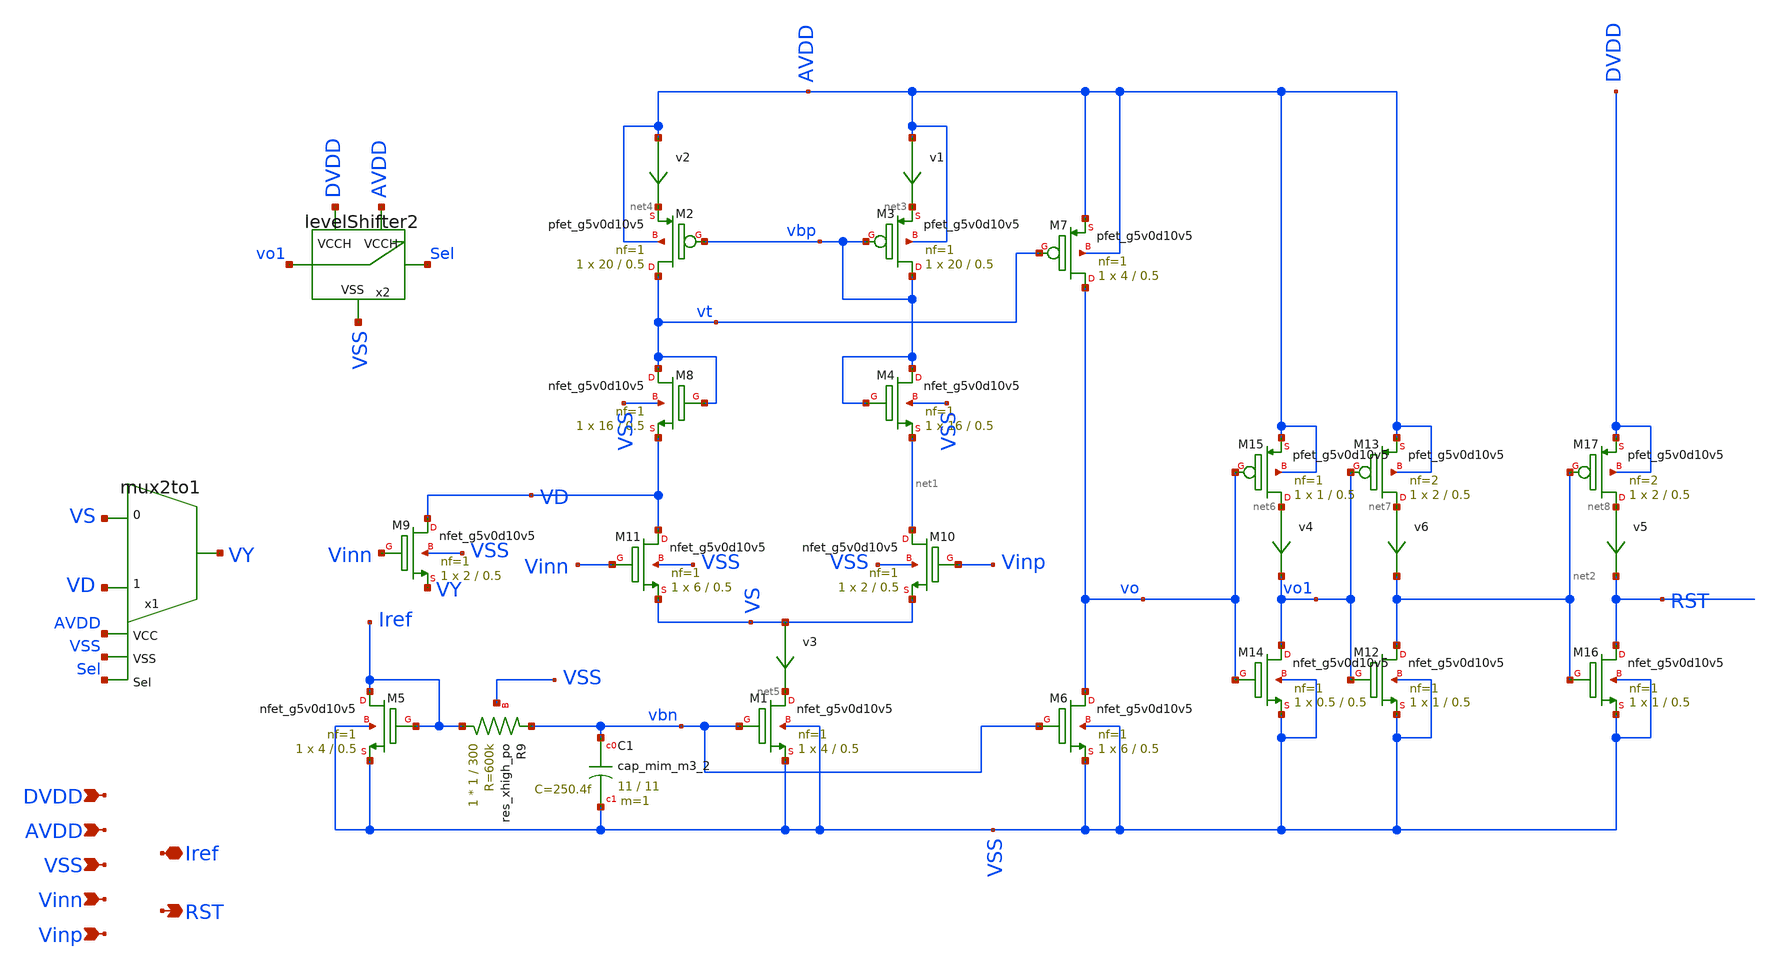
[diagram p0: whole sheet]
** sch_path: xschem/comparator_swu1.sch
**.subckt comparator_swu1 AVDD RST VSS Iref Vinn Vinp DVDD
*.ipin AVDD
*.opin RST
*.ipin VSS
*.iopin Iref
*.ipin Vinn
*.ipin Vinp
*.ipin DVDD
v1 AVDD net3 0
.save i(v1)
v2 AVDD net4 0
.save i(v2)
XM1 net5 vbn VSS VSS sky130_fd_pr__nfet_g5v0d10v5 L=0.5 W=4 nf=1 ad='int((nf+1)/2) * W/nf * 0.29' as='int((nf+2)/2) * W/nf * 0.29'
+ pd='2*int((nf+1)/2) * (W/nf + 0.29)' ps='2*int((nf+2)/2) * (W/nf + 0.29)' nrd='0.29 / W' nrs='0.29 / W'
+ sa=0 sb=0 sd=0 mult=1 m=1
XM3 vbp vbp net3 AVDD sky130_fd_pr__pfet_g5v0d10v5 L=0.5 W=20 nf=1 ad='int((nf+1)/2) * W/nf * 0.29' as='int((nf+2)/2) * W/nf * 0.29'
+ pd='2*int((nf+1)/2) * (W/nf + 0.29)' ps='2*int((nf+2)/2) * (W/nf + 0.29)' nrd='0.29 / W' nrs='0.29 / W'
+ sa=0 sb=0 sd=0 mult=1 m=1
XM2 vt vbp net4 AVDD sky130_fd_pr__pfet_g5v0d10v5 L=0.5 W=20 nf=1 ad='int((nf+1)/2) * W/nf * 0.29' as='int((nf+2)/2) * W/nf * 0.29'
+ pd='2*int((nf+1)/2) * (W/nf + 0.29)' ps='2*int((nf+2)/2) * (W/nf + 0.29)' nrd='0.29 / W' nrs='0.29 / W'
+ sa=0 sb=0 sd=0 mult=1 m=1
v4 net6 vo1 0
.save i(v4)
XM9 VD Vinn VY VSS sky130_fd_pr__nfet_g5v0d10v5 L=0.5 W=2 nf=1 ad='int((nf+1)/2) * W/nf * 0.29' as='int((nf+2)/2) * W/nf * 0.29'
+ pd='2*int((nf+1)/2) * (W/nf + 0.29)' ps='2*int((nf+2)/2) * (W/nf + 0.29)' nrd='0.29 / W' nrs='0.29 / W'
+ sa=0 sb=0 sd=0 mult=1 m=1
XM10 net1 Vinp VS VSS sky130_fd_pr__nfet_g5v0d10v5 L=0.5 W=2 nf=1 ad='int((nf+1)/2) * W/nf * 0.29' as='int((nf+2)/2) * W/nf * 0.29'
+ pd='2*int((nf+1)/2) * (W/nf + 0.29)' ps='2*int((nf+2)/2) * (W/nf + 0.29)' nrd='0.29 / W' nrs='0.29 / W'
+ sa=0 sb=0 sd=0 mult=1 m=1
XM5 Iref Iref VSS VSS sky130_fd_pr__nfet_g5v0d10v5 L=0.5 W=4 nf=1 ad='int((nf+1)/2) * W/nf * 0.29' as='int((nf+2)/2) * W/nf * 0.29'
+ pd='2*int((nf+1)/2) * (W/nf + 0.29)' ps='2*int((nf+2)/2) * (W/nf + 0.29)' nrd='0.29 / W' nrs='0.29 / W'
+ sa=0 sb=0 sd=0 mult=1 m=1
XM7 vo vt AVDD AVDD sky130_fd_pr__pfet_g5v0d10v5 L=0.5 W=4 nf=1 ad='int((nf+1)/2) * W/nf * 0.29' as='int((nf+2)/2) * W/nf * 0.29'
+ pd='2*int((nf+1)/2) * (W/nf + 0.29)' ps='2*int((nf+2)/2) * (W/nf + 0.29)' nrd='0.29 / W' nrs='0.29 / W'
+ sa=0 sb=0 sd=0 mult=1 m=1
v3 VS net5 0
.save i(v3)
XM11 VD Vinn VS VSS sky130_fd_pr__nfet_g5v0d10v5 L=0.5 W=6 nf=1 ad='int((nf+1)/2) * W/nf * 0.29' as='int((nf+2)/2) * W/nf * 0.29'
+ pd='2*int((nf+1)/2) * (W/nf + 0.29)' ps='2*int((nf+2)/2) * (W/nf + 0.29)' nrd='0.29 / W' nrs='0.29 / W'
+ sa=0 sb=0 sd=0 mult=1 m=1
x1 VD VS VY AVDD VSS Sel mux2to1
XM6 vo vbn VSS VSS sky130_fd_pr__nfet_g5v0d10v5 L=0.5 W=6 nf=1 ad='int((nf+1)/2) * W/nf * 0.29' as='int((nf+2)/2) * W/nf * 0.29'
+ pd='2*int((nf+1)/2) * (W/nf + 0.29)' ps='2*int((nf+2)/2) * (W/nf + 0.29)' nrd='0.29 / W' nrs='0.29 / W'
+ sa=0 sb=0 sd=0 mult=1 m=1
v6 net7 net2 0
.save i(v6)
XM14 vo1 vo VSS VSS sky130_fd_pr__nfet_g5v0d10v5 L=0.5 W=0.5 nf=1 ad='int((nf+1)/2) * W/nf * 0.29' as='int((nf+2)/2) * W/nf * 0.29'
+ pd='2*int((nf+1)/2) * (W/nf + 0.29)' ps='2*int((nf+2)/2) * (W/nf + 0.29)' nrd='0.29 / W' nrs='0.29 / W'
+ sa=0 sb=0 sd=0 mult=1 m=1
XM15 net6 vo AVDD AVDD sky130_fd_pr__pfet_g5v0d10v5 L=0.5 W=1 nf=1 ad='int((nf+1)/2) * W/nf * 0.29' as='int((nf+2)/2) * W/nf * 0.29'
+ pd='2*int((nf+1)/2) * (W/nf + 0.29)' ps='2*int((nf+2)/2) * (W/nf + 0.29)' nrd='0.29 / W' nrs='0.29 / W'
+ sa=0 sb=0 sd=0 mult=1 m=1
XM12 net2 vo1 VSS VSS sky130_fd_pr__nfet_g5v0d10v5 L=0.5 W=1 nf=1 ad='int((nf+1)/2) * W/nf * 0.29' as='int((nf+2)/2) * W/nf * 0.29'
+ pd='2*int((nf+1)/2) * (W/nf + 0.29)' ps='2*int((nf+2)/2) * (W/nf + 0.29)' nrd='0.29 / W' nrs='0.29 / W'
+ sa=0 sb=0 sd=0 mult=1 m=1
XM13 net7 vo1 AVDD AVDD sky130_fd_pr__pfet_g5v0d10v5 L=0.5 W=2 nf=2 ad='int((nf+1)/2) * W/nf * 0.29'
+ as='int((nf+2)/2) * W/nf * 0.29' pd='2*int((nf+1)/2) * (W/nf + 0.29)' ps='2*int((nf+2)/2) * (W/nf + 0.29)'
+ nrd='0.29 / W' nrs='0.29 / W' sa=0 sb=0 sd=0 mult=1 m=1
x2 vo1 Sel DVDD VSS AVDD levelShifter2
v5 net8 RST 0
.save i(v5)
XM16 RST net2 VSS VSS sky130_fd_pr__nfet_g5v0d10v5 L=0.5 W=1 nf=1 ad='int((nf+1)/2) * W/nf * 0.29' as='int((nf+2)/2) * W/nf * 0.29'
+ pd='2*int((nf+1)/2) * (W/nf + 0.29)' ps='2*int((nf+2)/2) * (W/nf + 0.29)' nrd='0.29 / W' nrs='0.29 / W'
+ sa=0 sb=0 sd=0 mult=1 m=1
XM17 net8 net2 DVDD DVDD sky130_fd_pr__pfet_g5v0d10v5 L=0.5 W=2 nf=2 ad='int((nf+1)/2) * W/nf * 0.29'
+ as='int((nf+2)/2) * W/nf * 0.29' pd='2*int((nf+1)/2) * (W/nf + 0.29)' ps='2*int((nf+2)/2) * (W/nf + 0.29)'
+ nrd='0.29 / W' nrs='0.29 / W' sa=0 sb=0 sd=0 mult=1 m=1
XC1 vbn VSS sky130_fd_pr__cap_mim_m3_2 W=11 L=11 MF=1 m=1
XM4 vbp vbp net1 VSS sky130_fd_pr__nfet_g5v0d10v5 L=0.5 W=16 nf=1 ad='int((nf+1)/2) * W/nf * 0.29' as='int((nf+2)/2) * W/nf * 0.29'
+ pd='2*int((nf+1)/2) * (W/nf + 0.29)' ps='2*int((nf+2)/2) * (W/nf + 0.29)' nrd='0.29 / W' nrs='0.29 / W'
+ sa=0 sb=0 sd=0 mult=1 m=1
XM8 vt vt VD VSS sky130_fd_pr__nfet_g5v0d10v5 L=0.5 W=16 nf=1 ad='int((nf+1)/2) * W/nf * 0.29' as='int((nf+2)/2) * W/nf * 0.29'
+ pd='2*int((nf+1)/2) * (W/nf + 0.29)' ps='2*int((nf+2)/2) * (W/nf + 0.29)' nrd='0.29 / W' nrs='0.29 / W'
+ sa=0 sb=0 sd=0 mult=1 m=1
XR9 Iref vbn VSS sky130_fd_pr__res_xhigh_po W=1 L=300 mult=1 m=1
**.ends
.end
